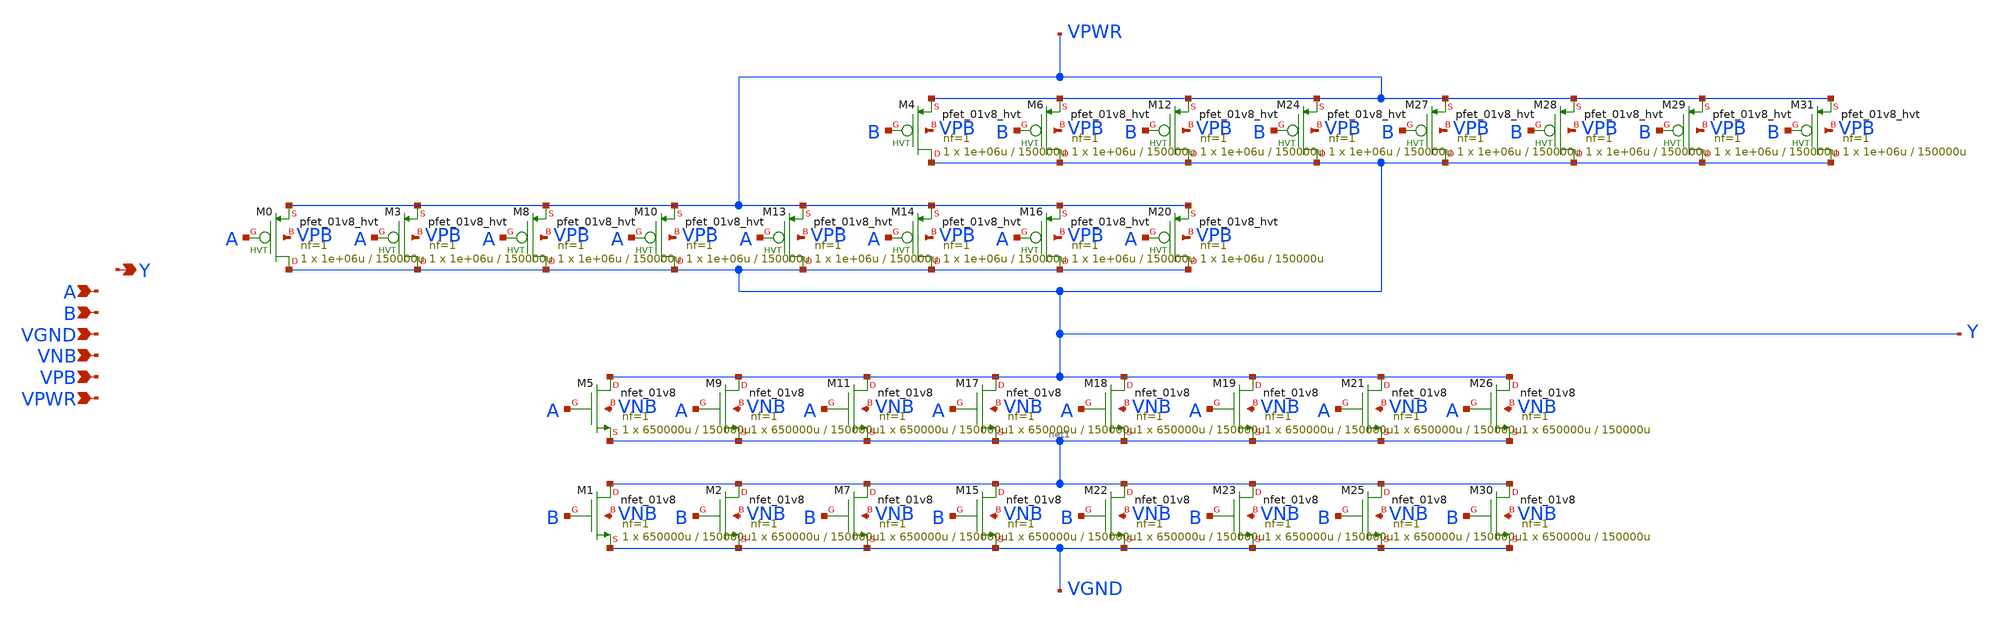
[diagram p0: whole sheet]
** sch_path: schematics/nand2/sky130_fd_sc_hd__nand2_8.sch
**.subckt sky130_fd_sc_hd__nand2_8 A B VGND VNB VPB VPWR Y
*.ipin A
*.ipin B
*.ipin VGND
*.ipin VNB
*.ipin VPB
*.ipin VPWR
*.opin Y
XM0 Y A VPWR VPB sky130_fd_pr__pfet_01v8_hvt L=150000u W=1e+06u nf=1 ad='int((1 + 1)/2) * 1e+06u / 1 * 0.29'
+ as='int((1 + 2)/2) * 1e+06u / 1 * 0.29' pd='2*int((1 + 1)/2) * (1e+06u / 1 + 0.29)' ps='2*int((1 + 2)/2) * (1e+06u / 1 + 0.29)'
+ nrd='0.29 / 1e+06u ' nrs='0.29 / 1e+06u ' sa=0 sb=0 sd=0 mult=1 m=1
XM3 Y A VPWR VPB sky130_fd_pr__pfet_01v8_hvt L=150000u W=1e+06u nf=1 ad='int((1 + 1)/2) * 1e+06u / 1 * 0.29'
+ as='int((1 + 2)/2) * 1e+06u / 1 * 0.29' pd='2*int((1 + 1)/2) * (1e+06u / 1 + 0.29)' ps='2*int((1 + 2)/2) * (1e+06u / 1 + 0.29)'
+ nrd='0.29 / 1e+06u ' nrs='0.29 / 1e+06u ' sa=0 sb=0 sd=0 mult=1 m=1
XM8 Y A VPWR VPB sky130_fd_pr__pfet_01v8_hvt L=150000u W=1e+06u nf=1 ad='int((1 + 1)/2) * 1e+06u / 1 * 0.29'
+ as='int((1 + 2)/2) * 1e+06u / 1 * 0.29' pd='2*int((1 + 1)/2) * (1e+06u / 1 + 0.29)' ps='2*int((1 + 2)/2) * (1e+06u / 1 + 0.29)'
+ nrd='0.29 / 1e+06u ' nrs='0.29 / 1e+06u ' sa=0 sb=0 sd=0 mult=1 m=1
XM10 Y A VPWR VPB sky130_fd_pr__pfet_01v8_hvt L=150000u W=1e+06u nf=1 ad='int((1 + 1)/2) * 1e+06u / 1 * 0.29'
+ as='int((1 + 2)/2) * 1e+06u / 1 * 0.29' pd='2*int((1 + 1)/2) * (1e+06u / 1 + 0.29)' ps='2*int((1 + 2)/2) * (1e+06u / 1 + 0.29)'
+ nrd='0.29 / 1e+06u ' nrs='0.29 / 1e+06u ' sa=0 sb=0 sd=0 mult=1 m=1
XM13 Y A VPWR VPB sky130_fd_pr__pfet_01v8_hvt L=150000u W=1e+06u nf=1 ad='int((1 + 1)/2) * 1e+06u / 1 * 0.29'
+ as='int((1 + 2)/2) * 1e+06u / 1 * 0.29' pd='2*int((1 + 1)/2) * (1e+06u / 1 + 0.29)' ps='2*int((1 + 2)/2) * (1e+06u / 1 + 0.29)'
+ nrd='0.29 / 1e+06u ' nrs='0.29 / 1e+06u ' sa=0 sb=0 sd=0 mult=1 m=1
XM14 Y A VPWR VPB sky130_fd_pr__pfet_01v8_hvt L=150000u W=1e+06u nf=1 ad='int((1 + 1)/2) * 1e+06u / 1 * 0.29'
+ as='int((1 + 2)/2) * 1e+06u / 1 * 0.29' pd='2*int((1 + 1)/2) * (1e+06u / 1 + 0.29)' ps='2*int((1 + 2)/2) * (1e+06u / 1 + 0.29)'
+ nrd='0.29 / 1e+06u ' nrs='0.29 / 1e+06u ' sa=0 sb=0 sd=0 mult=1 m=1
XM16 Y A VPWR VPB sky130_fd_pr__pfet_01v8_hvt L=150000u W=1e+06u nf=1 ad='int((1 + 1)/2) * 1e+06u / 1 * 0.29'
+ as='int((1 + 2)/2) * 1e+06u / 1 * 0.29' pd='2*int((1 + 1)/2) * (1e+06u / 1 + 0.29)' ps='2*int((1 + 2)/2) * (1e+06u / 1 + 0.29)'
+ nrd='0.29 / 1e+06u ' nrs='0.29 / 1e+06u ' sa=0 sb=0 sd=0 mult=1 m=1
XM20 Y A VPWR VPB sky130_fd_pr__pfet_01v8_hvt L=150000u W=1e+06u nf=1 ad='int((1 + 1)/2) * 1e+06u / 1 * 0.29'
+ as='int((1 + 2)/2) * 1e+06u / 1 * 0.29' pd='2*int((1 + 1)/2) * (1e+06u / 1 + 0.29)' ps='2*int((1 + 2)/2) * (1e+06u / 1 + 0.29)'
+ nrd='0.29 / 1e+06u ' nrs='0.29 / 1e+06u ' sa=0 sb=0 sd=0 mult=1 m=1
XM4 Y B VPWR VPB sky130_fd_pr__pfet_01v8_hvt L=150000u W=1e+06u nf=1 ad='int((1 + 1)/2) * 1e+06u / 1 * 0.29'
+ as='int((1 + 2)/2) * 1e+06u / 1 * 0.29' pd='2*int((1 + 1)/2) * (1e+06u / 1 + 0.29)' ps='2*int((1 + 2)/2) * (1e+06u / 1 + 0.29)'
+ nrd='0.29 / 1e+06u ' nrs='0.29 / 1e+06u ' sa=0 sb=0 sd=0 mult=1 m=1
XM6 Y B VPWR VPB sky130_fd_pr__pfet_01v8_hvt L=150000u W=1e+06u nf=1 ad='int((1 + 1)/2) * 1e+06u / 1 * 0.29'
+ as='int((1 + 2)/2) * 1e+06u / 1 * 0.29' pd='2*int((1 + 1)/2) * (1e+06u / 1 + 0.29)' ps='2*int((1 + 2)/2) * (1e+06u / 1 + 0.29)'
+ nrd='0.29 / 1e+06u ' nrs='0.29 / 1e+06u ' sa=0 sb=0 sd=0 mult=1 m=1
XM12 Y B VPWR VPB sky130_fd_pr__pfet_01v8_hvt L=150000u W=1e+06u nf=1 ad='int((1 + 1)/2) * 1e+06u / 1 * 0.29'
+ as='int((1 + 2)/2) * 1e+06u / 1 * 0.29' pd='2*int((1 + 1)/2) * (1e+06u / 1 + 0.29)' ps='2*int((1 + 2)/2) * (1e+06u / 1 + 0.29)'
+ nrd='0.29 / 1e+06u ' nrs='0.29 / 1e+06u ' sa=0 sb=0 sd=0 mult=1 m=1
XM24 Y B VPWR VPB sky130_fd_pr__pfet_01v8_hvt L=150000u W=1e+06u nf=1 ad='int((1 + 1)/2) * 1e+06u / 1 * 0.29'
+ as='int((1 + 2)/2) * 1e+06u / 1 * 0.29' pd='2*int((1 + 1)/2) * (1e+06u / 1 + 0.29)' ps='2*int((1 + 2)/2) * (1e+06u / 1 + 0.29)'
+ nrd='0.29 / 1e+06u ' nrs='0.29 / 1e+06u ' sa=0 sb=0 sd=0 mult=1 m=1
XM27 Y B VPWR VPB sky130_fd_pr__pfet_01v8_hvt L=150000u W=1e+06u nf=1 ad='int((1 + 1)/2) * 1e+06u / 1 * 0.29'
+ as='int((1 + 2)/2) * 1e+06u / 1 * 0.29' pd='2*int((1 + 1)/2) * (1e+06u / 1 + 0.29)' ps='2*int((1 + 2)/2) * (1e+06u / 1 + 0.29)'
+ nrd='0.29 / 1e+06u ' nrs='0.29 / 1e+06u ' sa=0 sb=0 sd=0 mult=1 m=1
XM28 Y B VPWR VPB sky130_fd_pr__pfet_01v8_hvt L=150000u W=1e+06u nf=1 ad='int((1 + 1)/2) * 1e+06u / 1 * 0.29'
+ as='int((1 + 2)/2) * 1e+06u / 1 * 0.29' pd='2*int((1 + 1)/2) * (1e+06u / 1 + 0.29)' ps='2*int((1 + 2)/2) * (1e+06u / 1 + 0.29)'
+ nrd='0.29 / 1e+06u ' nrs='0.29 / 1e+06u ' sa=0 sb=0 sd=0 mult=1 m=1
XM29 Y B VPWR VPB sky130_fd_pr__pfet_01v8_hvt L=150000u W=1e+06u nf=1 ad='int((1 + 1)/2) * 1e+06u / 1 * 0.29'
+ as='int((1 + 2)/2) * 1e+06u / 1 * 0.29' pd='2*int((1 + 1)/2) * (1e+06u / 1 + 0.29)' ps='2*int((1 + 2)/2) * (1e+06u / 1 + 0.29)'
+ nrd='0.29 / 1e+06u ' nrs='0.29 / 1e+06u ' sa=0 sb=0 sd=0 mult=1 m=1
XM31 Y B VPWR VPB sky130_fd_pr__pfet_01v8_hvt L=150000u W=1e+06u nf=1 ad='int((1 + 1)/2) * 1e+06u / 1 * 0.29'
+ as='int((1 + 2)/2) * 1e+06u / 1 * 0.29' pd='2*int((1 + 1)/2) * (1e+06u / 1 + 0.29)' ps='2*int((1 + 2)/2) * (1e+06u / 1 + 0.29)'
+ nrd='0.29 / 1e+06u ' nrs='0.29 / 1e+06u ' sa=0 sb=0 sd=0 mult=1 m=1
XM5 Y A net1 VNB sky130_fd_pr__nfet_01v8 L=150000u W=650000u nf=1 ad='int((1 + 1)/2) * 650000u / 1 * 0.29'
+ as='int((1 + 2)/2) * 650000u / 1 * 0.29' pd='2*int((1 + 1)/2) * (650000u / 1 + 0.29)' ps='2*int((1 + 2)/2) * (650000u / 1 + 0.29)'
+ nrd='0.29 / 650000u ' nrs='0.29 / 650000u ' sa=0 sb=0 sd=0 mult=1 m=1
XM9 Y A net1 VNB sky130_fd_pr__nfet_01v8 L=150000u W=650000u nf=1 ad='int((1 + 1)/2) * 650000u / 1 * 0.29'
+ as='int((1 + 2)/2) * 650000u / 1 * 0.29' pd='2*int((1 + 1)/2) * (650000u / 1 + 0.29)' ps='2*int((1 + 2)/2) * (650000u / 1 + 0.29)'
+ nrd='0.29 / 650000u ' nrs='0.29 / 650000u ' sa=0 sb=0 sd=0 mult=1 m=1
XM11 Y A net1 VNB sky130_fd_pr__nfet_01v8 L=150000u W=650000u nf=1 ad='int((1 + 1)/2) * 650000u / 1 * 0.29'
+ as='int((1 + 2)/2) * 650000u / 1 * 0.29' pd='2*int((1 + 1)/2) * (650000u / 1 + 0.29)' ps='2*int((1 + 2)/2) * (650000u / 1 + 0.29)'
+ nrd='0.29 / 650000u ' nrs='0.29 / 650000u ' sa=0 sb=0 sd=0 mult=1 m=1
XM17 Y A net1 VNB sky130_fd_pr__nfet_01v8 L=150000u W=650000u nf=1 ad='int((1 + 1)/2) * 650000u / 1 * 0.29'
+ as='int((1 + 2)/2) * 650000u / 1 * 0.29' pd='2*int((1 + 1)/2) * (650000u / 1 + 0.29)' ps='2*int((1 + 2)/2) * (650000u / 1 + 0.29)'
+ nrd='0.29 / 650000u ' nrs='0.29 / 650000u ' sa=0 sb=0 sd=0 mult=1 m=1
XM18 Y A net1 VNB sky130_fd_pr__nfet_01v8 L=150000u W=650000u nf=1 ad='int((1 + 1)/2) * 650000u / 1 * 0.29'
+ as='int((1 + 2)/2) * 650000u / 1 * 0.29' pd='2*int((1 + 1)/2) * (650000u / 1 + 0.29)' ps='2*int((1 + 2)/2) * (650000u / 1 + 0.29)'
+ nrd='0.29 / 650000u ' nrs='0.29 / 650000u ' sa=0 sb=0 sd=0 mult=1 m=1
XM19 Y A net1 VNB sky130_fd_pr__nfet_01v8 L=150000u W=650000u nf=1 ad='int((1 + 1)/2) * 650000u / 1 * 0.29'
+ as='int((1 + 2)/2) * 650000u / 1 * 0.29' pd='2*int((1 + 1)/2) * (650000u / 1 + 0.29)' ps='2*int((1 + 2)/2) * (650000u / 1 + 0.29)'
+ nrd='0.29 / 650000u ' nrs='0.29 / 650000u ' sa=0 sb=0 sd=0 mult=1 m=1
XM21 Y A net1 VNB sky130_fd_pr__nfet_01v8 L=150000u W=650000u nf=1 ad='int((1 + 1)/2) * 650000u / 1 * 0.29'
+ as='int((1 + 2)/2) * 650000u / 1 * 0.29' pd='2*int((1 + 1)/2) * (650000u / 1 + 0.29)' ps='2*int((1 + 2)/2) * (650000u / 1 + 0.29)'
+ nrd='0.29 / 650000u ' nrs='0.29 / 650000u ' sa=0 sb=0 sd=0 mult=1 m=1
XM26 Y A net1 VNB sky130_fd_pr__nfet_01v8 L=150000u W=650000u nf=1 ad='int((1 + 1)/2) * 650000u / 1 * 0.29'
+ as='int((1 + 2)/2) * 650000u / 1 * 0.29' pd='2*int((1 + 1)/2) * (650000u / 1 + 0.29)' ps='2*int((1 + 2)/2) * (650000u / 1 + 0.29)'
+ nrd='0.29 / 650000u ' nrs='0.29 / 650000u ' sa=0 sb=0 sd=0 mult=1 m=1
XM1 net1 B VGND VNB sky130_fd_pr__nfet_01v8 L=150000u W=650000u nf=1 ad='int((1 + 1)/2) * 650000u / 1 * 0.29'
+ as='int((1 + 2)/2) * 650000u / 1 * 0.29' pd='2*int((1 + 1)/2) * (650000u / 1 + 0.29)' ps='2*int((1 + 2)/2) * (650000u / 1 + 0.29)'
+ nrd='0.29 / 650000u ' nrs='0.29 / 650000u ' sa=0 sb=0 sd=0 mult=1 m=1
XM2 net1 B VGND VNB sky130_fd_pr__nfet_01v8 L=150000u W=650000u nf=1 ad='int((1 + 1)/2) * 650000u / 1 * 0.29'
+ as='int((1 + 2)/2) * 650000u / 1 * 0.29' pd='2*int((1 + 1)/2) * (650000u / 1 + 0.29)' ps='2*int((1 + 2)/2) * (650000u / 1 + 0.29)'
+ nrd='0.29 / 650000u ' nrs='0.29 / 650000u ' sa=0 sb=0 sd=0 mult=1 m=1
XM7 net1 B VGND VNB sky130_fd_pr__nfet_01v8 L=150000u W=650000u nf=1 ad='int((1 + 1)/2) * 650000u / 1 * 0.29'
+ as='int((1 + 2)/2) * 650000u / 1 * 0.29' pd='2*int((1 + 1)/2) * (650000u / 1 + 0.29)' ps='2*int((1 + 2)/2) * (650000u / 1 + 0.29)'
+ nrd='0.29 / 650000u ' nrs='0.29 / 650000u ' sa=0 sb=0 sd=0 mult=1 m=1
XM15 net1 B VGND VNB sky130_fd_pr__nfet_01v8 L=150000u W=650000u nf=1 ad='int((1 + 1)/2) * 650000u / 1 * 0.29'
+ as='int((1 + 2)/2) * 650000u / 1 * 0.29' pd='2*int((1 + 1)/2) * (650000u / 1 + 0.29)' ps='2*int((1 + 2)/2) * (650000u / 1 + 0.29)'
+ nrd='0.29 / 650000u ' nrs='0.29 / 650000u ' sa=0 sb=0 sd=0 mult=1 m=1
XM22 net1 B VGND VNB sky130_fd_pr__nfet_01v8 L=150000u W=650000u nf=1 ad='int((1 + 1)/2) * 650000u / 1 * 0.29'
+ as='int((1 + 2)/2) * 650000u / 1 * 0.29' pd='2*int((1 + 1)/2) * (650000u / 1 + 0.29)' ps='2*int((1 + 2)/2) * (650000u / 1 + 0.29)'
+ nrd='0.29 / 650000u ' nrs='0.29 / 650000u ' sa=0 sb=0 sd=0 mult=1 m=1
XM23 net1 B VGND VNB sky130_fd_pr__nfet_01v8 L=150000u W=650000u nf=1 ad='int((1 + 1)/2) * 650000u / 1 * 0.29'
+ as='int((1 + 2)/2) * 650000u / 1 * 0.29' pd='2*int((1 + 1)/2) * (650000u / 1 + 0.29)' ps='2*int((1 + 2)/2) * (650000u / 1 + 0.29)'
+ nrd='0.29 / 650000u ' nrs='0.29 / 650000u ' sa=0 sb=0 sd=0 mult=1 m=1
XM25 net1 B VGND VNB sky130_fd_pr__nfet_01v8 L=150000u W=650000u nf=1 ad='int((1 + 1)/2) * 650000u / 1 * 0.29'
+ as='int((1 + 2)/2) * 650000u / 1 * 0.29' pd='2*int((1 + 1)/2) * (650000u / 1 + 0.29)' ps='2*int((1 + 2)/2) * (650000u / 1 + 0.29)'
+ nrd='0.29 / 650000u ' nrs='0.29 / 650000u ' sa=0 sb=0 sd=0 mult=1 m=1
XM30 net1 B VGND VNB sky130_fd_pr__nfet_01v8 L=150000u W=650000u nf=1 ad='int((1 + 1)/2) * 650000u / 1 * 0.29'
+ as='int((1 + 2)/2) * 650000u / 1 * 0.29' pd='2*int((1 + 1)/2) * (650000u / 1 + 0.29)' ps='2*int((1 + 2)/2) * (650000u / 1 + 0.29)'
+ nrd='0.29 / 650000u ' nrs='0.29 / 650000u ' sa=0 sb=0 sd=0 mult=1 m=1
**.ends
.end
